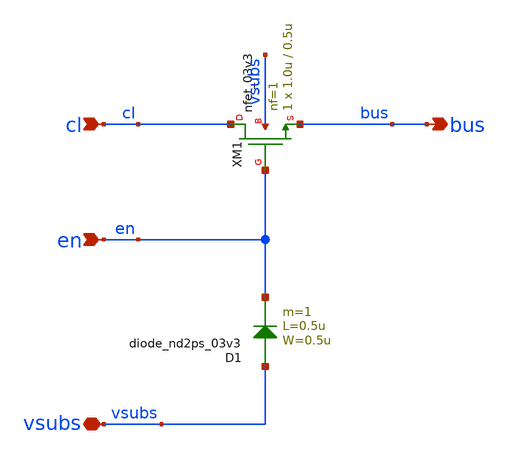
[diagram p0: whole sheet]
** sch_path: xschem/ip_column_switch.sch
**.subckt ip_column_switch cl en vsubs bus
*.ipin cl
*.ipin en
*.iopin vsubs
*.opin bus
XM1 cl en bus vsubs nfet_03v3 L=0.5u W=1.0u nf=1 ad='int((nf+1)/2) * W/nf * 0.18u' as='int((nf+2)/2) * W/nf * 0.18u'
+ pd='2*int((nf+1)/2) * (W/nf + 0.18u)' ps='2*int((nf+2)/2) * (W/nf + 0.18u)' nrd='0.18u / W' nrs='0.18u / W'
+ sa=0 sb=0 sd=0 m=1
D1 vsubs en diode_nd2ps_03v3 area='0.5u * 0.5u ' pj='2*0.5u + 2*0.5u ' m=1
**.ends
.end
